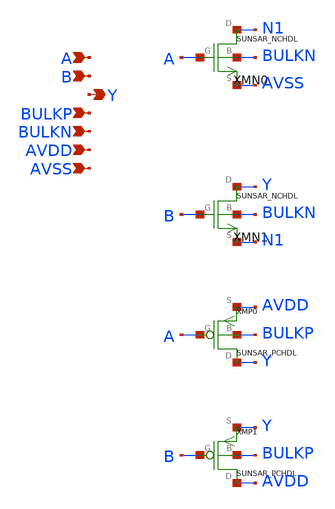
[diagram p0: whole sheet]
** sch_path: ip/sun_sar9b_sky130nm/design/SUN_SAR9B_SKY130NM/SUNSAR_NDX1_CV.sch
**.subckt SUNSAR_NDX1_CV A B Y BULKP BULKN AVDD AVSS
*.ipin A
*.ipin B
*.opin Y
*.ipin BULKP
*.ipin BULKN
*.ipin AVDD
*.ipin AVSS
XMN0 N1 A AVSS BULKN SUNSAR_NCHDL
XMN1 Y B N1 BULKN SUNSAR_NCHDL
XMP0 Y A AVDD BULKP SUNSAR_PCHDL
XMP1 AVDD B Y BULKP SUNSAR_PCHDL
**.ends
.end
